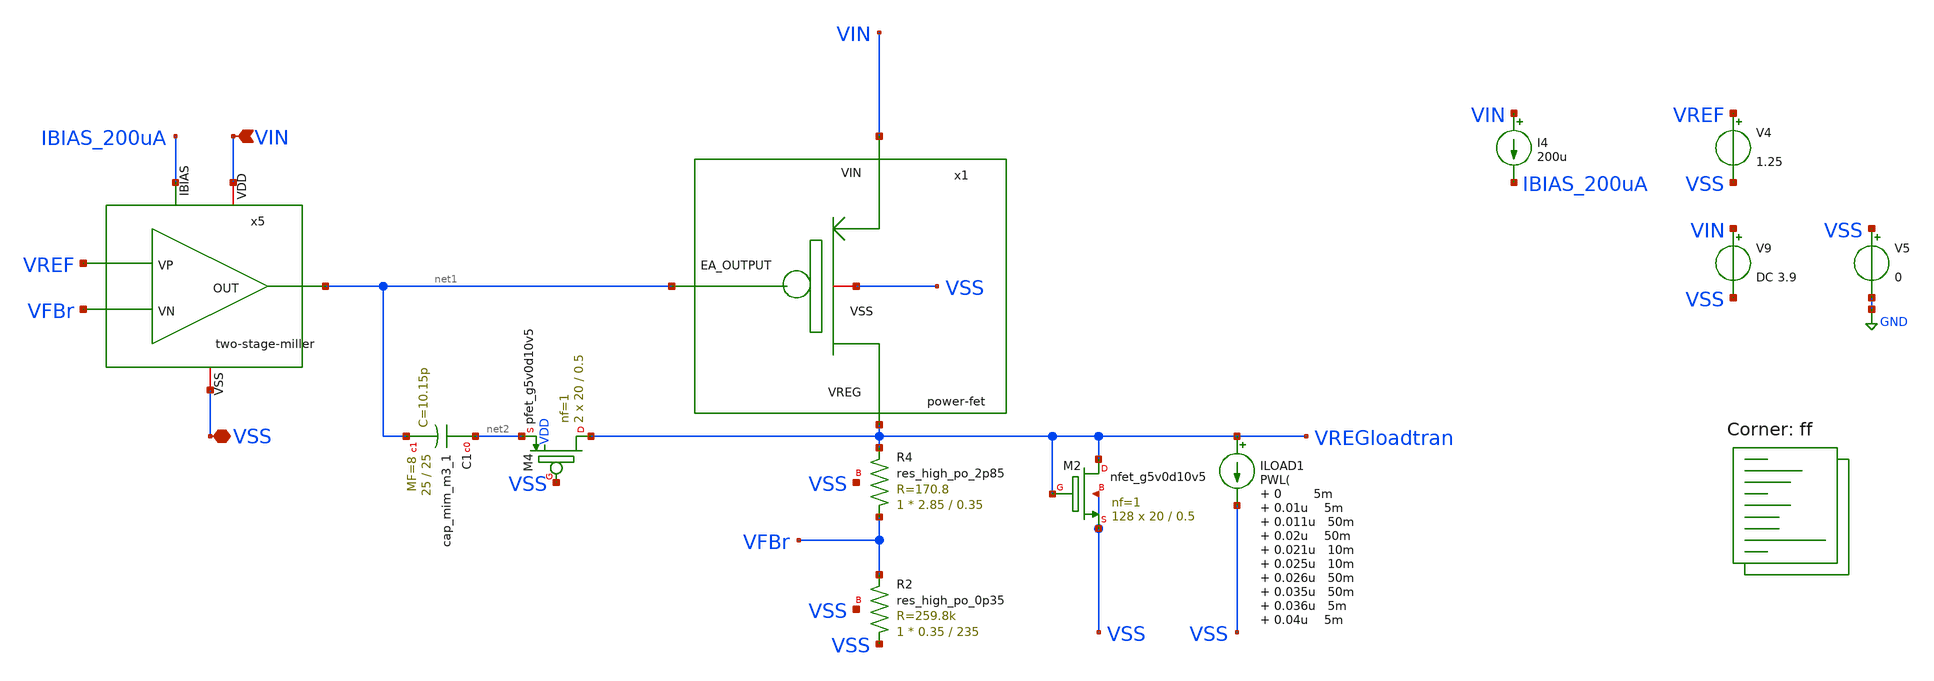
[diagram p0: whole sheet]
** sch_path: bandgap/testbench/tb_tran_medium.sch
**.subckt tb_tran_medium VIN VSS
*.ipin VIN
*.iopin VSS
I4 VIN IBIAS_200uA 200u
V4 VREF VSS 1.25
V5 VSS GND 0
V9 VIN VSS DC 3.9
x1 VIN VSS net1 VREGloadtran power-fet
XR2 VSS VFBr VSS sky130_fd_pr__res_high_po_0p35 L=235 mult=1 m=1
XR4 VFBr VREGloadtran VSS sky130_fd_pr__res_high_po_2p85 L=0.35 mult=1 m=1
x5 VIN net1 VREF VFBr IBIAS_200uA VSS two-stage-miller
ILOAD1 VREGloadtran VSS PWL( 0 5m 0.01u 5m 0.011u 50m 0.02u 50m 0.021u 10m 0.025u 10m 0.026u 50m
+ 0.035u 50m 0.036u 5m 0.04u 5m
)
XC1 net2 net1 sky130_fd_pr__cap_mim_m3_1 W=25 L=25 MF=8 m=8
XM4 VREGloadtran VSS net2 VDD sky130_fd_pr__pfet_g5v0d10v5 L=0.5 W=20 nf=1 ad='int((nf+1)/2) * W/nf * 0.29'
+ as='int((nf+2)/2) * W/nf * 0.29' pd='2*int((nf+1)/2) * (W/nf + 0.29)' ps='2*int((nf+2)/2) * (W/nf + 0.29)'
+ nrd='0.29 / W' nrs='0.29 / W' sa=0 sb=0 sd=0 mult=2 m=2
XM2 VREGloadtran VREGloadtran VSS VSS sky130_fd_pr__nfet_g5v0d10v5 L=0.5 W=20 nf=1 ad='int((nf+1)/2) * W/nf * 0.29'
+ as='int((nf+2)/2) * W/nf * 0.29' pd='2*int((nf+1)/2) * (W/nf + 0.29)' ps='2*int((nf+2)/2) * (W/nf + 0.29)'
+ nrd='0.29 / W' nrs='0.29 / W' sa=0 sb=0 sd=0 mult=128 m=128
**** begin user architecture code



.temp 175
.control

tran 0.001n 0.08u

* Nominal output voltage (from regulation region)
let Vout_nom = 1.25
let Vout_95  = 0.95*Vout_nom

* Find Vin where Vout crosses 95%
meas dc Vin_do find v(vin) when v(vreg)=Vout_95

* Measure Vout at that Vin (for completeness)
meas dc Vout_do find v(vreg) when v(vreg)=Vout_95

* Compute dropout voltage
let Vdo = Vin_do - Vout_do

* Compute overshoot, undershoot and peak-to-peak voltage
meas tran Vout_max MAX v(VREGloadtran)
meas tran Vout_min MIN v(VREGloadtran)
let vpp = Vout_max - Vout_min

*Compute PSRR
meas ac psrr_dc  param= -20*log10(mag(v(VREGac)))  at=1
meas ac psrr_100k  param= -20*log10(mag(v(VREGac)))  at=100k
meas ac psrr_1M  param= -20*log10(mag(v(VREGaz)))  at=1Meg

* --- Settling Time Measurement Block ---
let v_final = 1.25  ; Target Vout
let tol = 0.01 * v_final
let hi_bound = v_final + tol
let lo_bound = v_final - tol

* 1. FIXED TRIGGER: We know the PWL starts the rise at 50ns
let t_trigger = 50n

* 2. Find the LAST time the signal was outside the tolerance band
* We measure after the step occurs (after 50ns)
meas tran t_last_hi WHEN v(VREGloadtran)=hi_bound FALL=LAST
meas tran t_last_lo WHEN v(VREGloadtran)=lo_bound RISE=LAST

* 3. Calculate Settling Time
* Ensure we only look at crossings that happened AFTER the trigger
let t_settle_end = max(t_last_hi, t_last_lo)
let settling_time = t_settle_end - t_trigger

print settling_time


print Vin_do Vout_do Vdo
print Vout_max Vout_min Vpp
plot VREGloadtran
plot VREGloadtran2
plot VREG
plot VIN
plot I(Vmeas)

.endc


.lib $::SKYWATER_MODELS/sky130.lib.spice ff
**** end user architecture code
**.ends
.GLOBAL GND
.end
